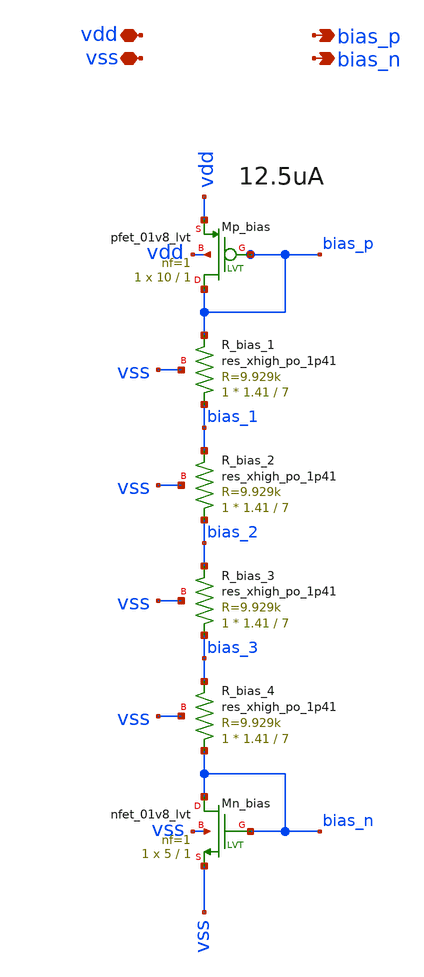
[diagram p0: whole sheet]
** sch_path: xsch/ip/vbias_generation/vbias_generation.sch
**.subckt vbias_generation bias_p vdd vss bias_n
*.opin bias_p
*.iopin vdd
*.iopin vss
*.opin bias_n
XR_bias_1 bias_1 bias_p vss sky130_fd_pr__res_xhigh_po_1p41 L=7 mult=1 m=1
XMn_bias bias_n bias_n vss vss sky130_fd_pr__nfet_01v8_lvt L=1 W=5 nf=1 ad='int((nf+1)/2) * W/nf * 0.29'
+ as='int((nf+2)/2) * W/nf * 0.29' pd='2*int((nf+1)/2) * (W/nf + 0.29)' ps='2*int((nf+2)/2) * (W/nf + 0.29)'
+ nrd='0.29 / W' nrs='0.29 / W' sa=0 sb=0 sd=0 mult=1 m=1
XMp_bias bias_p bias_p vdd vdd sky130_fd_pr__pfet_01v8_lvt L=1 W=10 nf=1 ad='int((nf+1)/2) * W/nf * 0.29'
+ as='int((nf+2)/2) * W/nf * 0.29' pd='2*int((nf+1)/2) * (W/nf + 0.29)' ps='2*int((nf+2)/2) * (W/nf + 0.29)'
+ nrd='0.29 / W' nrs='0.29 / W' sa=0 sb=0 sd=0 mult=1 m=1
XR_bias_2 bias_2 bias_1 vss sky130_fd_pr__res_xhigh_po_1p41 L=7 mult=1 m=1
XR_bias_3 bias_3 bias_2 vss sky130_fd_pr__res_xhigh_po_1p41 L=7 mult=1 m=1
XR_bias_4 bias_n bias_3 vss sky130_fd_pr__res_xhigh_po_1p41 L=7 mult=1 m=1
**.ends
.end
